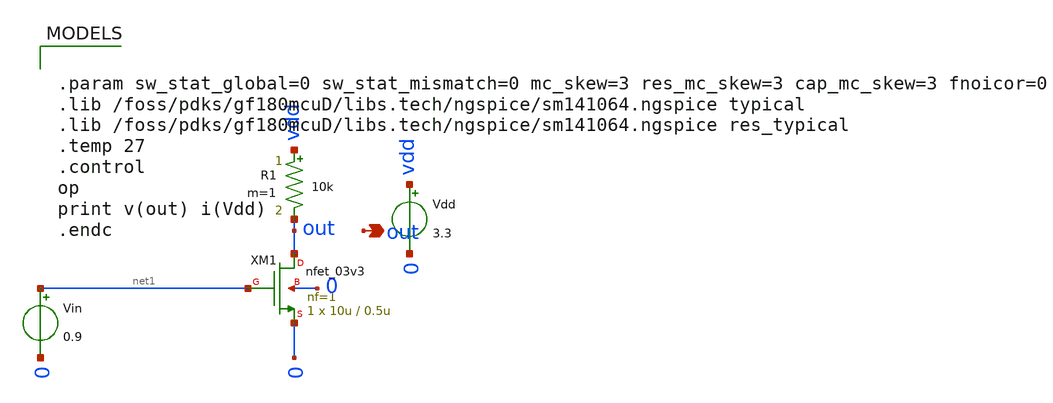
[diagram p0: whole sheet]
** sch_path: analog/lvds_rx/xschem/smoke/cs_stage.sch
**.subckt cs_stage out
*.opin out
XM1 out net1 0 0 nfet_03v3 L=0.5u W=10u nf=1 ad='int((nf+1)/2) * W/nf * 0.18u' as='int((nf+2)/2) * W/nf * 0.18u'
+ pd='2*int((nf+1)/2) * (W/nf + 0.18u)' ps='2*int((nf+2)/2) * (W/nf + 0.18u)' nrd='0.18u / W' nrs='0.18u / W'
+ sa=0 sb=0 sd=0 m=1
R1 vdd out 10k m=1
Vin net1 0 0.9
Vdd vdd 0 3.3
**** begin user architecture code


.param sw_stat_global=0 sw_stat_mismatch=0 mc_skew=3 res_mc_skew=3 cap_mc_skew=3 fnoicor=0
.lib /foss/pdks/gf180mcuD/libs.tech/ngspice/sm141064.ngspice typical
.lib /foss/pdks/gf180mcuD/libs.tech/ngspice/sm141064.ngspice res_typical
.temp 27
.control
op
print v(out) i(Vdd)
.endc


**** end user architecture code
**.ends
.end
